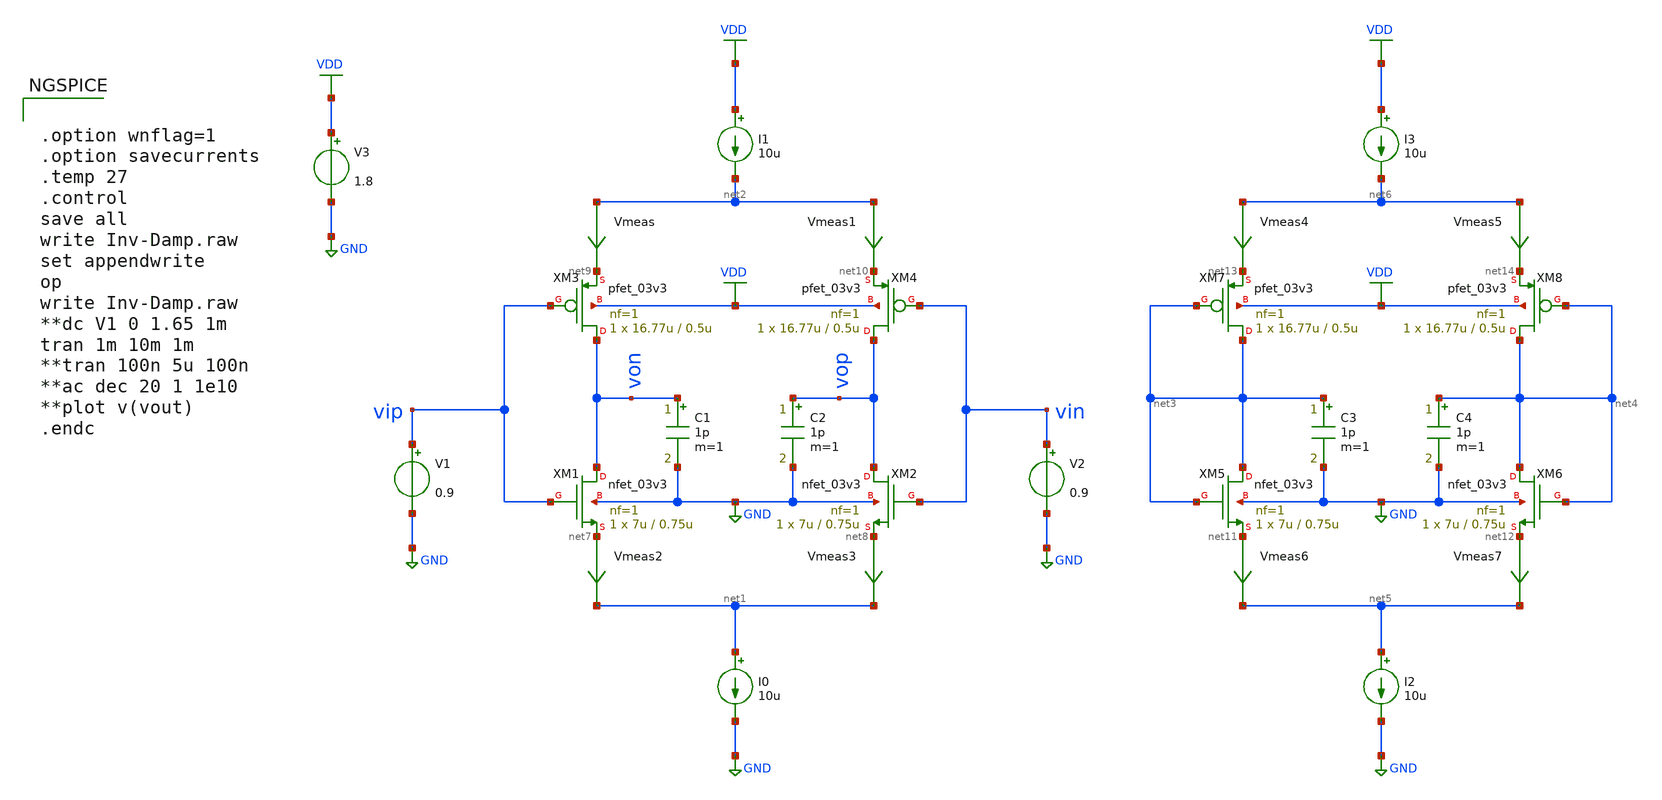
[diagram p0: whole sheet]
** sch_path: Design_Files/inverter-diff-amp/Inv-Damp.sch
**.subckt Inv-Damp
XM1 von vip net7 GND nfet_03v3 L=0.75u W=7u nf=1 ad='int((nf+1)/2) * W/nf * 0.18u' as='int((nf+2)/2) * W/nf * 0.18u'
+ pd='2*int((nf+1)/2) * (W/nf + 0.18u)' ps='2*int((nf+2)/2) * (W/nf + 0.18u)' nrd='0.18u / W' nrs='0.18u / W'
+ sa=0 sb=0 sd=0 m=1
XM2 vop vin net8 GND nfet_03v3 L=0.75u W=7u nf=1 ad='int((nf+1)/2) * W/nf * 0.18u' as='int((nf+2)/2) * W/nf * 0.18u'
+ pd='2*int((nf+1)/2) * (W/nf + 0.18u)' ps='2*int((nf+2)/2) * (W/nf + 0.18u)' nrd='0.18u / W' nrs='0.18u / W'
+ sa=0 sb=0 sd=0 m=1
XM3 von vip net9 VDD pfet_03v3 L=0.5u W=16.77u nf=1 ad='int((nf+1)/2) * W/nf * 0.18u' as='int((nf+2)/2) * W/nf * 0.18u'
+ pd='2*int((nf+1)/2) * (W/nf + 0.18u)' ps='2*int((nf+2)/2) * (W/nf + 0.18u)' nrd='0.18u / W' nrs='0.18u / W'
+ sa=0 sb=0 sd=0 m=1
XM4 vop vin net10 VDD pfet_03v3 L=0.5u W=16.77u nf=1 ad='int((nf+1)/2) * W/nf * 0.18u' as='int((nf+2)/2) * W/nf * 0.18u'
+ pd='2*int((nf+1)/2) * (W/nf + 0.18u)' ps='2*int((nf+2)/2) * (W/nf + 0.18u)' nrd='0.18u / W' nrs='0.18u / W'
+ sa=0 sb=0 sd=0 m=1
I0 net1 GND 10u
I1 VDD net2 10u
V1 vip GND 0.9
C1 von GND 1p m=1
C2 vop GND 1p m=1
V2 vin GND 0.9
V3 VDD GND 1.8
Vmeas net2 net9 0
.save i(vmeas)
Vmeas1 net2 net10 0
.save i(vmeas1)
Vmeas2 net7 net1 0
.save i(vmeas2)
Vmeas3 net8 net1 0
.save i(vmeas3)
XM5 net3 net3 net11 GND nfet_03v3 L=0.75u W=7u nf=1 ad='int((nf+1)/2) * W/nf * 0.18u' as='int((nf+2)/2) * W/nf * 0.18u'
+ pd='2*int((nf+1)/2) * (W/nf + 0.18u)' ps='2*int((nf+2)/2) * (W/nf + 0.18u)' nrd='0.18u / W' nrs='0.18u / W'
+ sa=0 sb=0 sd=0 m=1
XM6 net4 net4 net12 GND nfet_03v3 L=0.75u W=7u nf=1 ad='int((nf+1)/2) * W/nf * 0.18u' as='int((nf+2)/2) * W/nf * 0.18u'
+ pd='2*int((nf+1)/2) * (W/nf + 0.18u)' ps='2*int((nf+2)/2) * (W/nf + 0.18u)' nrd='0.18u / W' nrs='0.18u / W'
+ sa=0 sb=0 sd=0 m=1
XM7 net3 net3 net13 VDD pfet_03v3 L=0.5u W=16.77u nf=1 ad='int((nf+1)/2) * W/nf * 0.18u' as='int((nf+2)/2) * W/nf * 0.18u'
+ pd='2*int((nf+1)/2) * (W/nf + 0.18u)' ps='2*int((nf+2)/2) * (W/nf + 0.18u)' nrd='0.18u / W' nrs='0.18u / W'
+ sa=0 sb=0 sd=0 m=1
XM8 net4 net4 net14 VDD pfet_03v3 L=0.5u W=16.77u nf=1 ad='int((nf+1)/2) * W/nf * 0.18u' as='int((nf+2)/2) * W/nf * 0.18u'
+ pd='2*int((nf+1)/2) * (W/nf + 0.18u)' ps='2*int((nf+2)/2) * (W/nf + 0.18u)' nrd='0.18u / W' nrs='0.18u / W'
+ sa=0 sb=0 sd=0 m=1
I2 net5 GND 10u
I3 VDD net6 10u
C3 net3 GND 1p m=1
C4 net4 GND 1p m=1
Vmeas4 net6 net13 0
.save i(vmeas4)
Vmeas5 net6 net14 0
.save i(vmeas5)
Vmeas6 net11 net5 0
.save i(vmeas6)
Vmeas7 net12 net5 0
.save i(vmeas7)
**** begin user architecture code


.option wnflag=1
.option savecurrents
.temp 27
.control
save all
write Inv-Damp.raw
set appendwrite
op
write Inv-Damp.raw
**dc V1 0 1.65 1m
tran 1m 10m 1m
**tran 100n 5u 100n
**ac dec 20 1 1e10
**plot v(vout)
.endc




.lib /foss/pdks/volare/gf180mcu/versions/0fe599b2afb6708d281543108caf8310912f54af/gf180mcuD/libs.tech/ngspice/sm141064.ngspice typical
.include /foss/pdks/volare/gf180mcu/versions/0fe599b2afb6708d281543108caf8310912f54af/gf180mcuD/libs.tech/ngspice/design.ngspice

*.include $::180MCU_MODELS/design.ngspice
*.lib $::180MCU_MODELS/sm141064.ngspice typical




.save @m.xm1.m0[gm]
.save @m.xm1.m0[id]
.save @m.xm1.m0[vth]
.save @m.xm1.m0[gds]
.save @m.xm1.m0[cgg]
.save @m.xm1.m0[cgs]
.save @m.xm1.m0[cgd]
.save @m.xm2.m0[gm]
.save @m.xm2.m0[id]
.save @m.xm2.m0[vth]
.save @m.xm2.m0[gds]
.save @m.xm2.m0[cgg]
.save @m.xm2.m0[cgs]
.save @m.xm2.m0[cgd]
.save @m.xm3.m0[gm]
.save @m.xm3.m0[id]
.save @m.xm3.m0[vth]
.save @m.xm3.m0[gds]
.save @m.xm3.m0[cgg]
.save @m.xm3.m0[cgs]
.save @m.xm3.m0[cgd]
.save @m.xm4.m0[gm]
.save @m.xm4.m0[id]
.save @m.xm4.m0[vth]
.save @m.xm4.m0[gds]
.save @m.xm4.m0[cgg]
.save @m.xm4.m0[cgs]
.save @m.xm4.m0[cgd]


**** end user architecture code
**.ends
.GLOBAL GND
.GLOBAL VDD
.end
